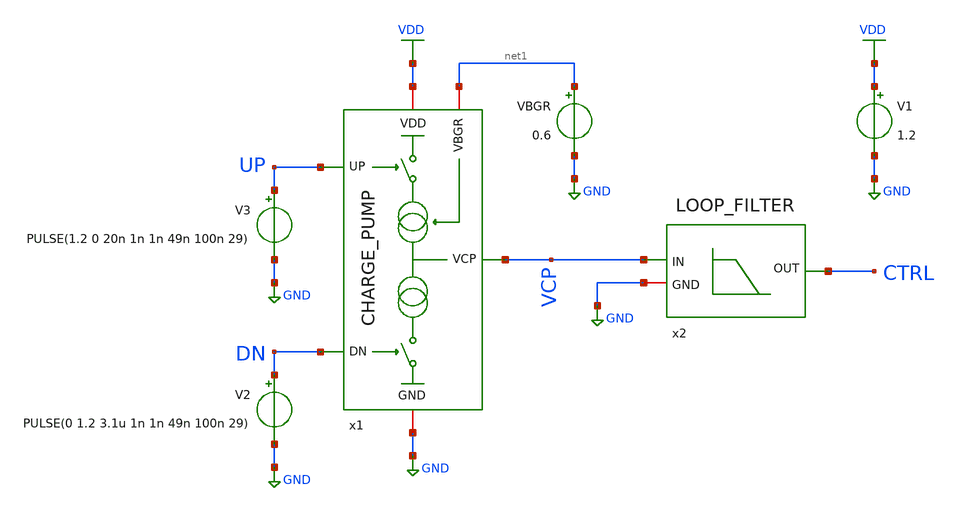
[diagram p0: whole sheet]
** sch_path: schematic/charge-pump/tb_CP_LF.sch
**.subckt tb_CP_LF
V1 VDD GND 1.2
V2 DN GND PULSE(0 1.2 3.1u 1n 1n 49n 100n 29)
V3 UP GND PULSE(1.2 0 20n 1n 1n 49n 100n 29)
VBGR net1 GND 0.6
x1 UP VDD VCP net1 GND DN CHARGE_PUMP
x2 CTRL VCP GND LOOP_FILTER
**** begin user architecture code



.include tb_CP.save
.param temp=27
.option method=gear rshunt=1.0e12
.control
save all
op
write tb_CP_LF.raw
.endc




.lib cornerMOSlv.lib mos_tt
.lib cornerMOShv.lib mos_tt
.lib cornerRES.lib res_typ
.lib cornerCAP.lib cap_typ




.param temp = 27
.options method=gear rshunt=1.0e12

.control

* Save required signals
save v(UP) v(DN) v(VCP) v(CTRL)

* Long transient simulation
tran 1n 6u

* Plot transient waveform
plot v(UP) v(DN) v(VCP) v(CTRL)
plot v(CTRL)

.endc



**** end user architecture code
**.ends

* expanding   symbol:
*+  /foss/designs/uniccass-icdesign-tools/shared_xserver/frac-n-pll-vco-smacd_2026/schematic/charge-pump/CHARGE_PUMP.sym # of pins=6
** sym_path: schematic/charge-pump/CHARGE_PUMP.sym
** sch_path: schematic/charge-pump/CHARGE_PUMP.sch
.subckt CHARGE_PUMP UP VDD VCP VBGR GND DN
*.opin VCP
*.ipin UP
*.ipin DN
*.iopin GND
*.iopin VBGR
*.iopin VDD
XM2 Vbn Vbn net5 GND sg13_lv_nmos w=40.7u l=2u ng=5 m=1 mm_ok=1
XM8 net2 GND VDD VDD sg13_lv_pmos w=29.6u l=2u ng=5 m=1 mm_ok=1
XM11 Vbp Vbp net2 VDD sg13_lv_pmos w=163.6u l=2u ng=20 m=1 mm_ok=1
XM3 Vbn Vbp net1 VDD sg13_lv_pmos w=163.6u l=2u ng=20 m=1 mm_ok=1
XM4 net1 GND VDD VDD sg13_lv_pmos w=29.6u l=2u ng=5 m=1 mm_ok=1
XM7 net3 UP VDD VDD sg13_lv_pmos w=29.6u l=2u ng=5 m=1 mm_ok=1
XM9 VCP Vbp net3 VDD sg13_lv_pmos w=163.6u l=2u ng=20 m=1 mm_ok=1
XM10 net5 VDD GND GND sg13_lv_nmos w=6u l=2u ng=1 m=1 mm_ok=1
XM1 net4 DN GND GND sg13_lv_nmos w=6u l=2u ng=1 m=1 mm_ok=1
XM5 VCP Vbn net4 GND sg13_lv_nmos w=40.7u l=2u ng=5 m=1 mm_ok=1
XM6 Vbp VBGR GND GND sg13_lv_nmos w=3.9u l=2u ng=1 m=1 mm_ok=1
.ends


* expanding   symbol:
*+  /foss/designs/uniccass-icdesign-tools/shared_xserver/frac-n-pll-vco-smacd_2026/schematic/loop-filter/LOOP_FILTER.sym # of pins=3
** sym_path: schematic/loop-filter/LOOP_FILTER.sym
** sch_path: schematic/loop-filter/LOOP_FILTER.sch
.subckt LOOP_FILTER OUT IN GND
*.opin OUT
*.iopin GND
*.ipin IN
XC2 OUT GND cap_cmim w=18.63e-6 l=18.63e-6 m=4 mm_ok=1
XC1 net1 GND cap_cmim w=48.34e-6 l=48.34e-6 m=16 mm_ok=1
XR2 OUT IN sub! rppd w=2e-6 l=407.22e-6 m=1 b=0 mm_ok=1
XR1 net1 IN sub! rppd w=2e-6 l=407.22e-6 m=1 b=0 mm_ok=1
.ends

.GLOBAL VDD
.GLOBAL GND
.end
